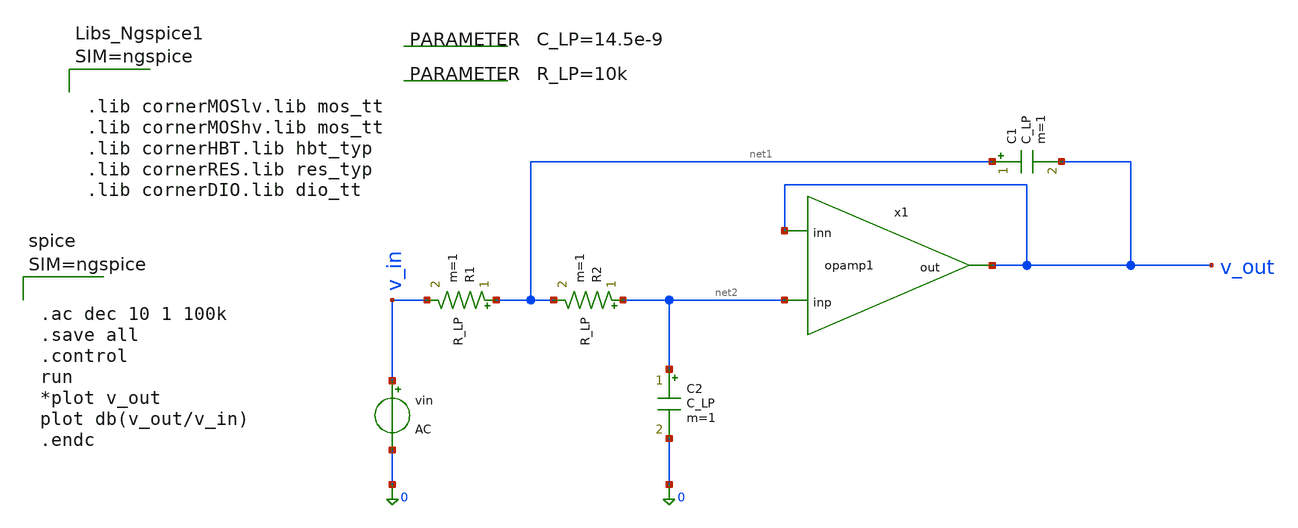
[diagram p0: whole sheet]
** sch_path: 003_Ideal_Circuits/sallen_key_opamp_ac.sch
**.subckt sallen_key_opamp_ac
R1 net1 v_in R_LP m=1
R2 net2 net1 R_LP m=1
C1 net1 v_out C_LP m=1
C2 net2 0 C_LP m=1
vin v_in 0 AC
.param C_LP=14.5e-9
.param R_LP=10k
x1 net2 v_out v_out opamp1
**** begin user architecture code



.lib cornerMOSlv.lib mos_tt
.lib cornerMOShv.lib mos_tt
.lib cornerHBT.lib hbt_typ
.lib cornerRES.lib res_typ
.lib cornerDIO.lib dio_tt






.ac dec 10 1 100k
.save all
.control
run
*plot v_out
plot db(v_out/v_in)
.endc



**** end user architecture code
**.ends

* expanding   symbol:  001_provided_files/2_Idealized_circuits/opamp1.sym # of pins=3
** sym_path: 001_provided_files/2_Idealized_circuits/opamp1.sym
** sch_path: 001_provided_files/2_Idealized_circuits/opamp1.sch
.subckt opamp1 inp inn out
*.ipin inp
*.ipin inn
*.opin out
Rin inp inn 10MEG m=1
Rout net2 out 10 m=1
Cp net1 GND 1.59u m=1
Rp GND net1 1k m=1
Ebuf net2 GND net1 GND 1
G1 net1 GND inp inn 1
.ends

.GLOBAL GND
.end
